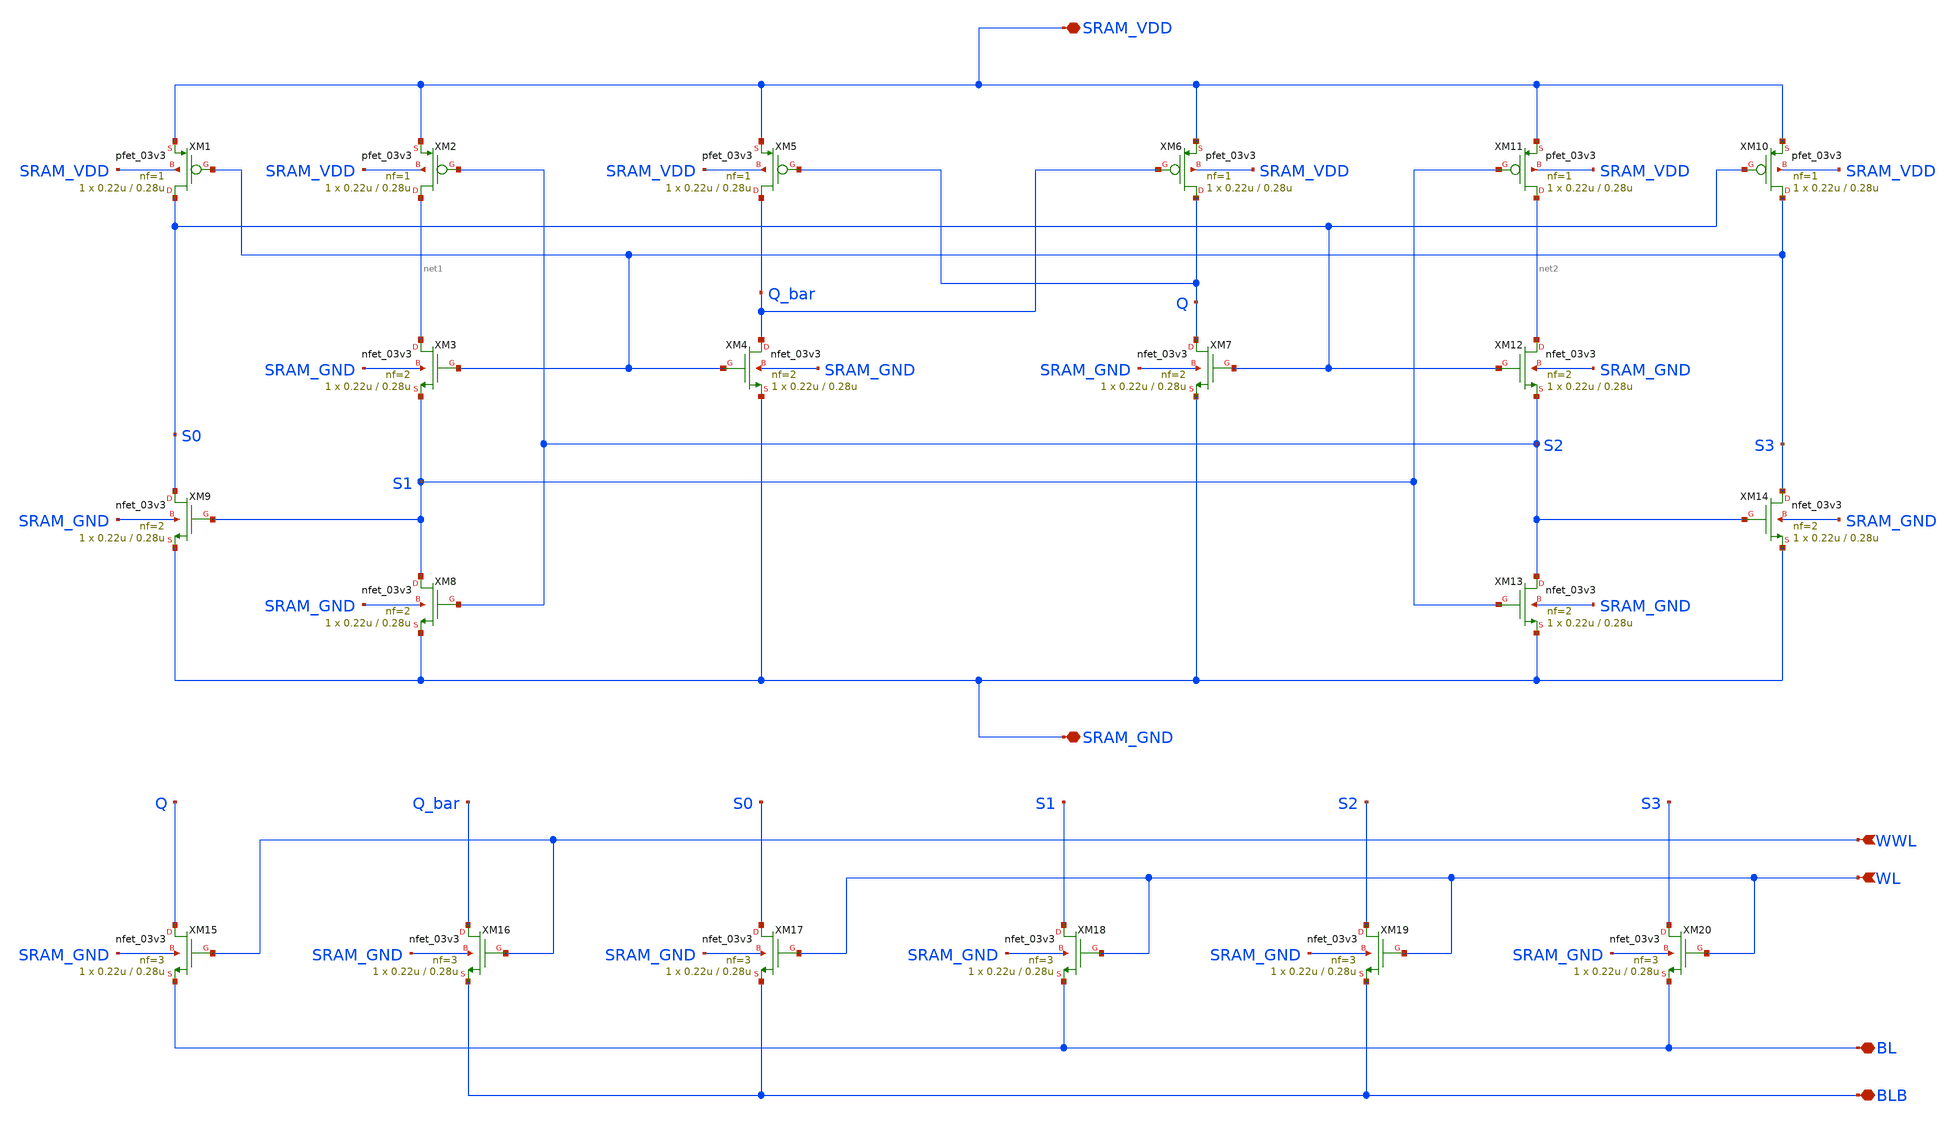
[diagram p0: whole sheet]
** sch_path: bitcell/RHRSE20T.sch
**.subckt RHRSE20T WWL WL SRAM_VDD SRAM_GND BL BLB
*.ipin WWL
*.ipin WL
*.iopin SRAM_VDD
*.iopin SRAM_GND
*.iopin BL
*.iopin BLB
XM1 S0 S3 SRAM_VDD SRAM_VDD pfet_03v3 L=0.28u W=0.22u nf=1 ad='int((nf+1)/2) * W/nf * 0.18u' as='int((nf+2)/2) * W/nf * 0.18u'
+ pd='2*int((nf+1)/2) * (W/nf + 0.18u)' ps='2*int((nf+2)/2) * (W/nf + 0.18u)' nrd='0.18u / W' nrs='0.18u / W'
+ sa=0 sb=0 sd=0 m=1
XM2 net1 S2 SRAM_VDD SRAM_VDD pfet_03v3 L=0.28u W=0.22u nf=1 ad='int((nf+1)/2) * W/nf * 0.18u' as='int((nf+2)/2) * W/nf * 0.18u'
+ pd='2*int((nf+1)/2) * (W/nf + 0.18u)' ps='2*int((nf+2)/2) * (W/nf + 0.18u)' nrd='0.18u / W' nrs='0.18u / W'
+ sa=0 sb=0 sd=0 m=1
XM3 net1 S3 S1 SRAM_GND nfet_03v3 L=0.28u W=0.22u nf=2 ad='int((nf+1)/2) * W/nf * 0.18u' as='int((nf+2)/2) * W/nf * 0.18u'
+ pd='2*int((nf+1)/2) * (W/nf + 0.18u)' ps='2*int((nf+2)/2) * (W/nf + 0.18u)' nrd='0.18u / W' nrs='0.18u / W'
+ sa=0 sb=0 sd=0 m=1
XM4 Q_bar S3 SRAM_GND SRAM_GND nfet_03v3 L=0.28u W=0.22u nf=2 ad='int((nf+1)/2) * W/nf * 0.18u' as='int((nf+2)/2) * W/nf * 0.18u'
+ pd='2*int((nf+1)/2) * (W/nf + 0.18u)' ps='2*int((nf+2)/2) * (W/nf + 0.18u)' nrd='0.18u / W' nrs='0.18u / W'
+ sa=0 sb=0 sd=0 m=1
XM5 Q_bar Q SRAM_VDD SRAM_VDD pfet_03v3 L=0.28u W=0.22u nf=1 ad='int((nf+1)/2) * W/nf * 0.18u' as='int((nf+2)/2) * W/nf * 0.18u'
+ pd='2*int((nf+1)/2) * (W/nf + 0.18u)' ps='2*int((nf+2)/2) * (W/nf + 0.18u)' nrd='0.18u / W' nrs='0.18u / W'
+ sa=0 sb=0 sd=0 m=1
XM6 Q Q_bar SRAM_VDD SRAM_VDD pfet_03v3 L=0.28u W=0.22u nf=1 ad='int((nf+1)/2) * W/nf * 0.18u' as='int((nf+2)/2) * W/nf * 0.18u'
+ pd='2*int((nf+1)/2) * (W/nf + 0.18u)' ps='2*int((nf+2)/2) * (W/nf + 0.18u)' nrd='0.18u / W' nrs='0.18u / W'
+ sa=0 sb=0 sd=0 m=1
XM7 Q S0 SRAM_GND SRAM_GND nfet_03v3 L=0.28u W=0.22u nf=2 ad='int((nf+1)/2) * W/nf * 0.18u' as='int((nf+2)/2) * W/nf * 0.18u'
+ pd='2*int((nf+1)/2) * (W/nf + 0.18u)' ps='2*int((nf+2)/2) * (W/nf + 0.18u)' nrd='0.18u / W' nrs='0.18u / W'
+ sa=0 sb=0 sd=0 m=1
XM8 S1 S2 SRAM_GND SRAM_GND nfet_03v3 L=0.28u W=0.22u nf=2 ad='int((nf+1)/2) * W/nf * 0.18u' as='int((nf+2)/2) * W/nf * 0.18u'
+ pd='2*int((nf+1)/2) * (W/nf + 0.18u)' ps='2*int((nf+2)/2) * (W/nf + 0.18u)' nrd='0.18u / W' nrs='0.18u / W'
+ sa=0 sb=0 sd=0 m=1
XM9 S0 S1 SRAM_GND SRAM_GND nfet_03v3 L=0.28u W=0.22u nf=2 ad='int((nf+1)/2) * W/nf * 0.18u' as='int((nf+2)/2) * W/nf * 0.18u'
+ pd='2*int((nf+1)/2) * (W/nf + 0.18u)' ps='2*int((nf+2)/2) * (W/nf + 0.18u)' nrd='0.18u / W' nrs='0.18u / W'
+ sa=0 sb=0 sd=0 m=1
XM10 S3 S0 SRAM_VDD SRAM_VDD pfet_03v3 L=0.28u W=0.22u nf=1 ad='int((nf+1)/2) * W/nf * 0.18u' as='int((nf+2)/2) * W/nf * 0.18u'
+ pd='2*int((nf+1)/2) * (W/nf + 0.18u)' ps='2*int((nf+2)/2) * (W/nf + 0.18u)' nrd='0.18u / W' nrs='0.18u / W'
+ sa=0 sb=0 sd=0 m=1
XM11 net2 S1 SRAM_VDD SRAM_VDD pfet_03v3 L=0.28u W=0.22u nf=1 ad='int((nf+1)/2) * W/nf * 0.18u' as='int((nf+2)/2) * W/nf * 0.18u'
+ pd='2*int((nf+1)/2) * (W/nf + 0.18u)' ps='2*int((nf+2)/2) * (W/nf + 0.18u)' nrd='0.18u / W' nrs='0.18u / W'
+ sa=0 sb=0 sd=0 m=1
XM12 net2 S0 S2 SRAM_GND nfet_03v3 L=0.28u W=0.22u nf=2 ad='int((nf+1)/2) * W/nf * 0.18u' as='int((nf+2)/2) * W/nf * 0.18u'
+ pd='2*int((nf+1)/2) * (W/nf + 0.18u)' ps='2*int((nf+2)/2) * (W/nf + 0.18u)' nrd='0.18u / W' nrs='0.18u / W'
+ sa=0 sb=0 sd=0 m=1
XM13 S2 S1 SRAM_GND SRAM_GND nfet_03v3 L=0.28u W=0.22u nf=2 ad='int((nf+1)/2) * W/nf * 0.18u' as='int((nf+2)/2) * W/nf * 0.18u'
+ pd='2*int((nf+1)/2) * (W/nf + 0.18u)' ps='2*int((nf+2)/2) * (W/nf + 0.18u)' nrd='0.18u / W' nrs='0.18u / W'
+ sa=0 sb=0 sd=0 m=1
XM14 S3 S2 SRAM_GND SRAM_GND nfet_03v3 L=0.28u W=0.22u nf=2 ad='int((nf+1)/2) * W/nf * 0.18u' as='int((nf+2)/2) * W/nf * 0.18u'
+ pd='2*int((nf+1)/2) * (W/nf + 0.18u)' ps='2*int((nf+2)/2) * (W/nf + 0.18u)' nrd='0.18u / W' nrs='0.18u / W'
+ sa=0 sb=0 sd=0 m=1
XM15 Q WWL BL SRAM_GND nfet_03v3 L=0.28u W=0.22u nf=3 ad='int((nf+1)/2) * W/nf * 0.18u' as='int((nf+2)/2) * W/nf * 0.18u'
+ pd='2*int((nf+1)/2) * (W/nf + 0.18u)' ps='2*int((nf+2)/2) * (W/nf + 0.18u)' nrd='0.18u / W' nrs='0.18u / W'
+ sa=0 sb=0 sd=0 m=1
XM16 Q_bar WWL BLB SRAM_GND nfet_03v3 L=0.28u W=0.22u nf=3 ad='int((nf+1)/2) * W/nf * 0.18u' as='int((nf+2)/2) * W/nf * 0.18u'
+ pd='2*int((nf+1)/2) * (W/nf + 0.18u)' ps='2*int((nf+2)/2) * (W/nf + 0.18u)' nrd='0.18u / W' nrs='0.18u / W'
+ sa=0 sb=0 sd=0 m=1
XM17 S0 WL BLB SRAM_GND nfet_03v3 L=0.28u W=0.22u nf=3 ad='int((nf+1)/2) * W/nf * 0.18u' as='int((nf+2)/2) * W/nf * 0.18u'
+ pd='2*int((nf+1)/2) * (W/nf + 0.18u)' ps='2*int((nf+2)/2) * (W/nf + 0.18u)' nrd='0.18u / W' nrs='0.18u / W'
+ sa=0 sb=0 sd=0 m=1
XM18 S1 WL BL SRAM_GND nfet_03v3 L=0.28u W=0.22u nf=3 ad='int((nf+1)/2) * W/nf * 0.18u' as='int((nf+2)/2) * W/nf * 0.18u'
+ pd='2*int((nf+1)/2) * (W/nf + 0.18u)' ps='2*int((nf+2)/2) * (W/nf + 0.18u)' nrd='0.18u / W' nrs='0.18u / W'
+ sa=0 sb=0 sd=0 m=1
XM19 S2 WL BLB SRAM_GND nfet_03v3 L=0.28u W=0.22u nf=3 ad='int((nf+1)/2) * W/nf * 0.18u' as='int((nf+2)/2) * W/nf * 0.18u'
+ pd='2*int((nf+1)/2) * (W/nf + 0.18u)' ps='2*int((nf+2)/2) * (W/nf + 0.18u)' nrd='0.18u / W' nrs='0.18u / W'
+ sa=0 sb=0 sd=0 m=1
XM20 S3 WL BL SRAM_GND nfet_03v3 L=0.28u W=0.22u nf=3 ad='int((nf+1)/2) * W/nf * 0.18u' as='int((nf+2)/2) * W/nf * 0.18u'
+ pd='2*int((nf+1)/2) * (W/nf + 0.18u)' ps='2*int((nf+2)/2) * (W/nf + 0.18u)' nrd='0.18u / W' nrs='0.18u / W'
+ sa=0 sb=0 sd=0 m=1
**.ends
.end
